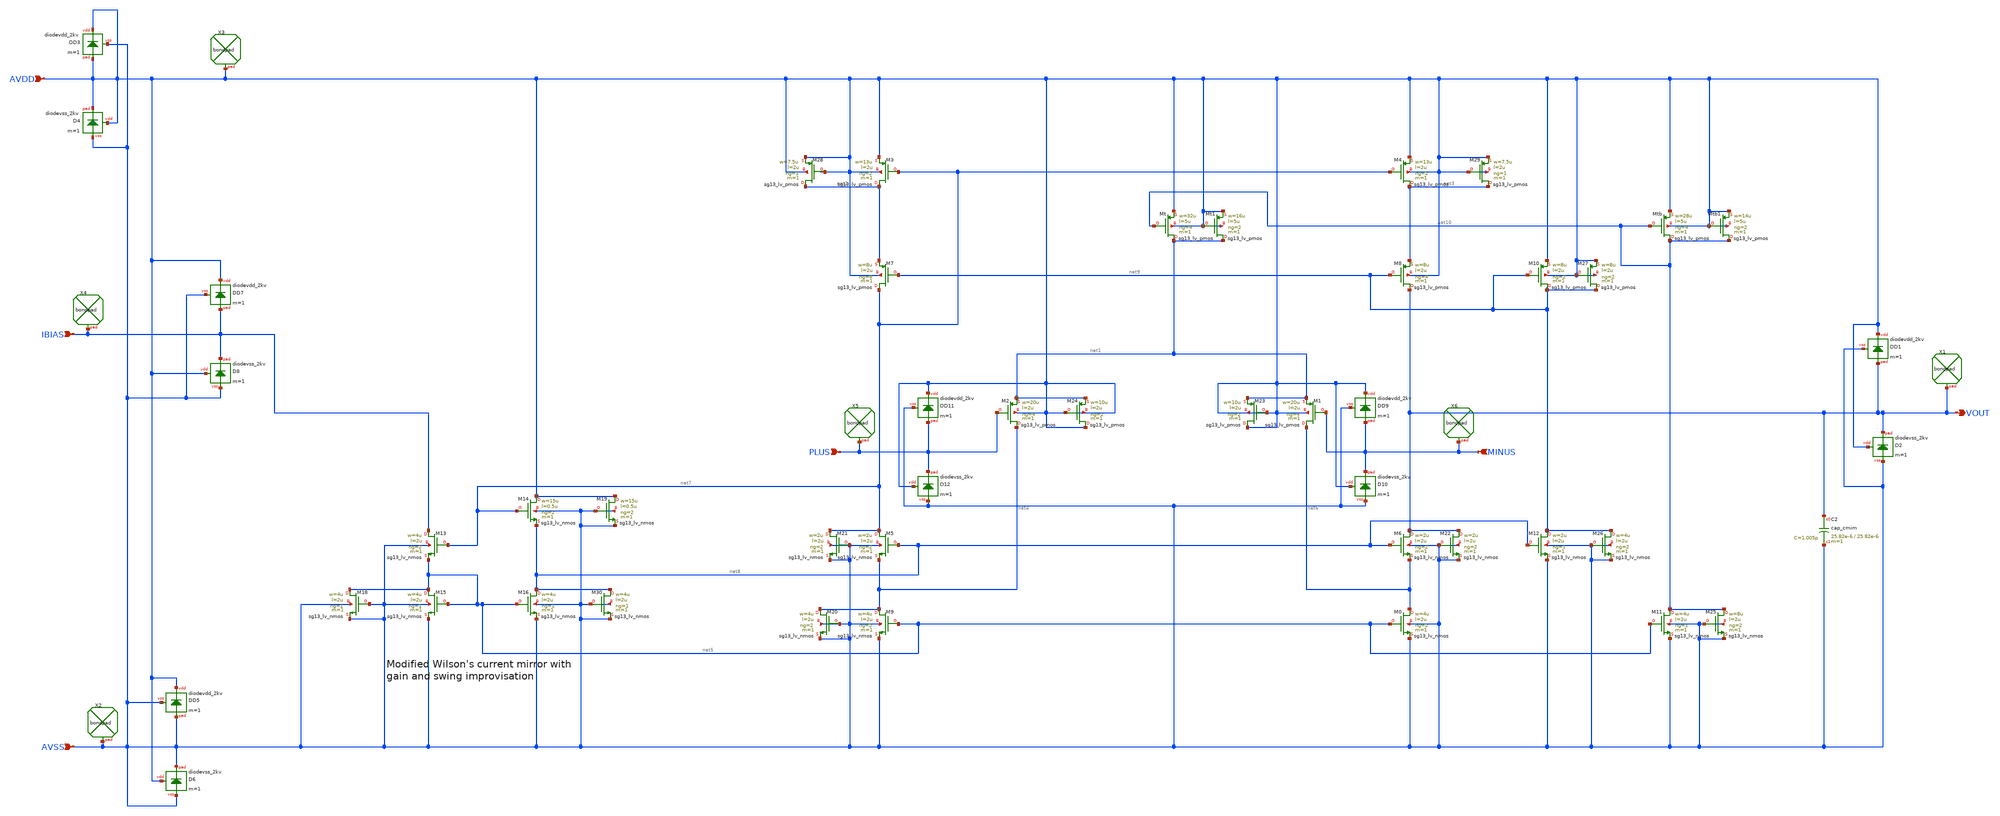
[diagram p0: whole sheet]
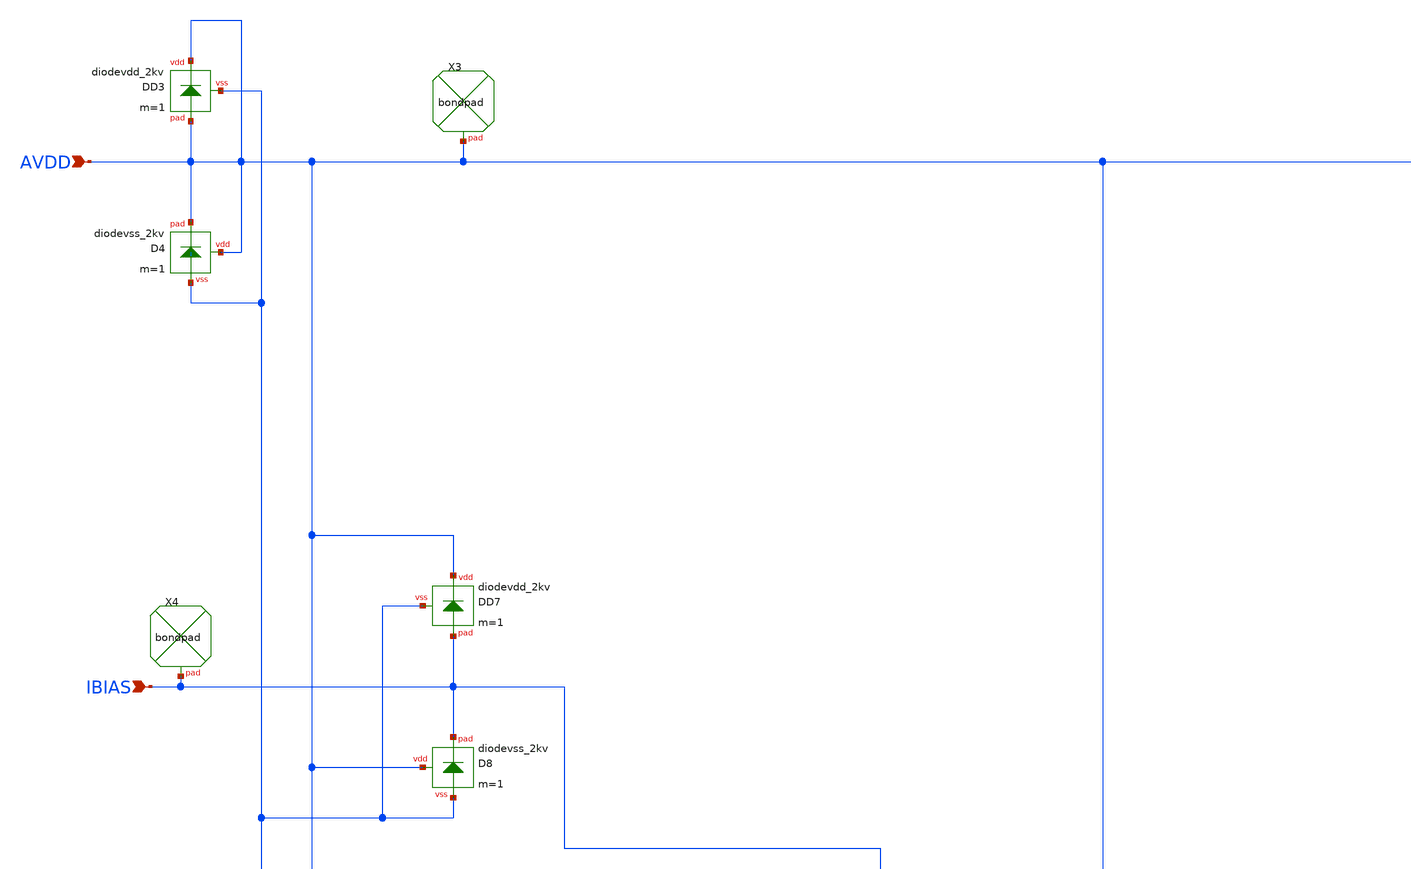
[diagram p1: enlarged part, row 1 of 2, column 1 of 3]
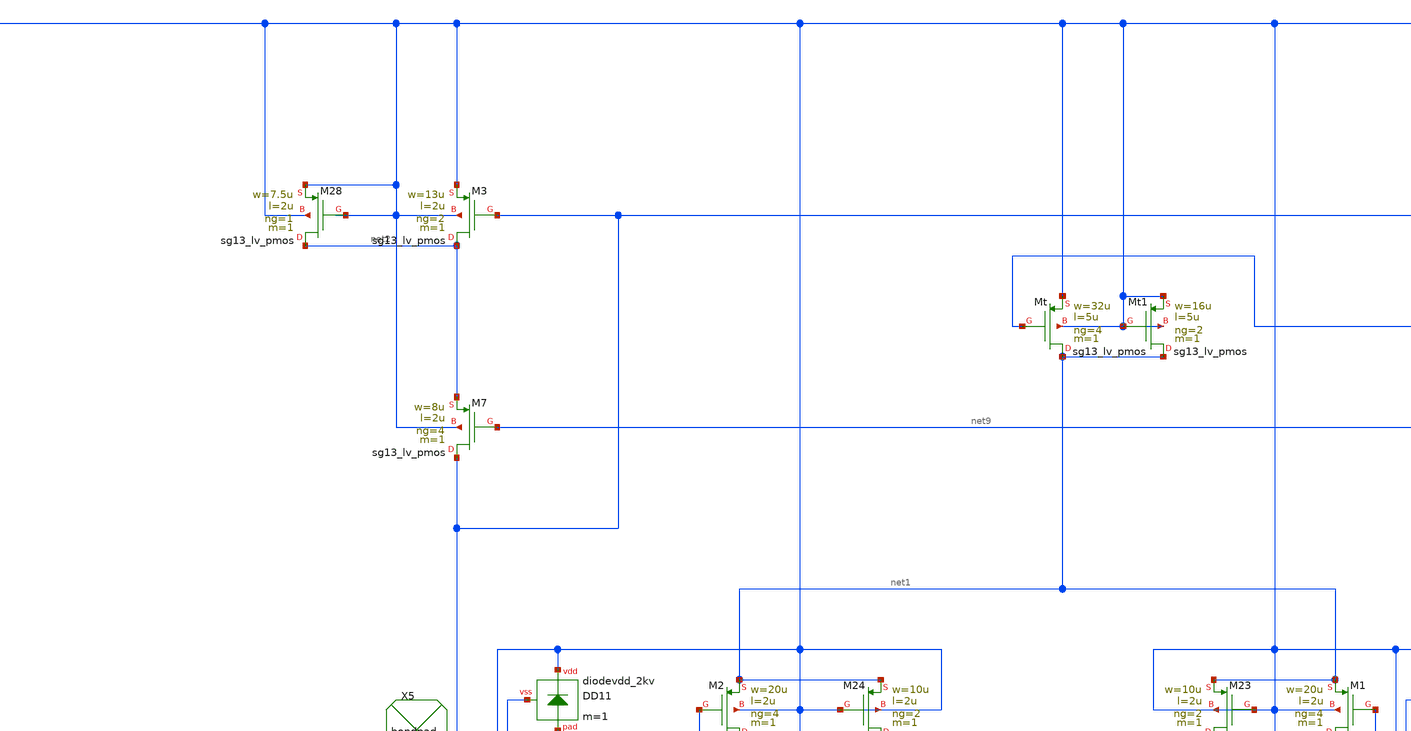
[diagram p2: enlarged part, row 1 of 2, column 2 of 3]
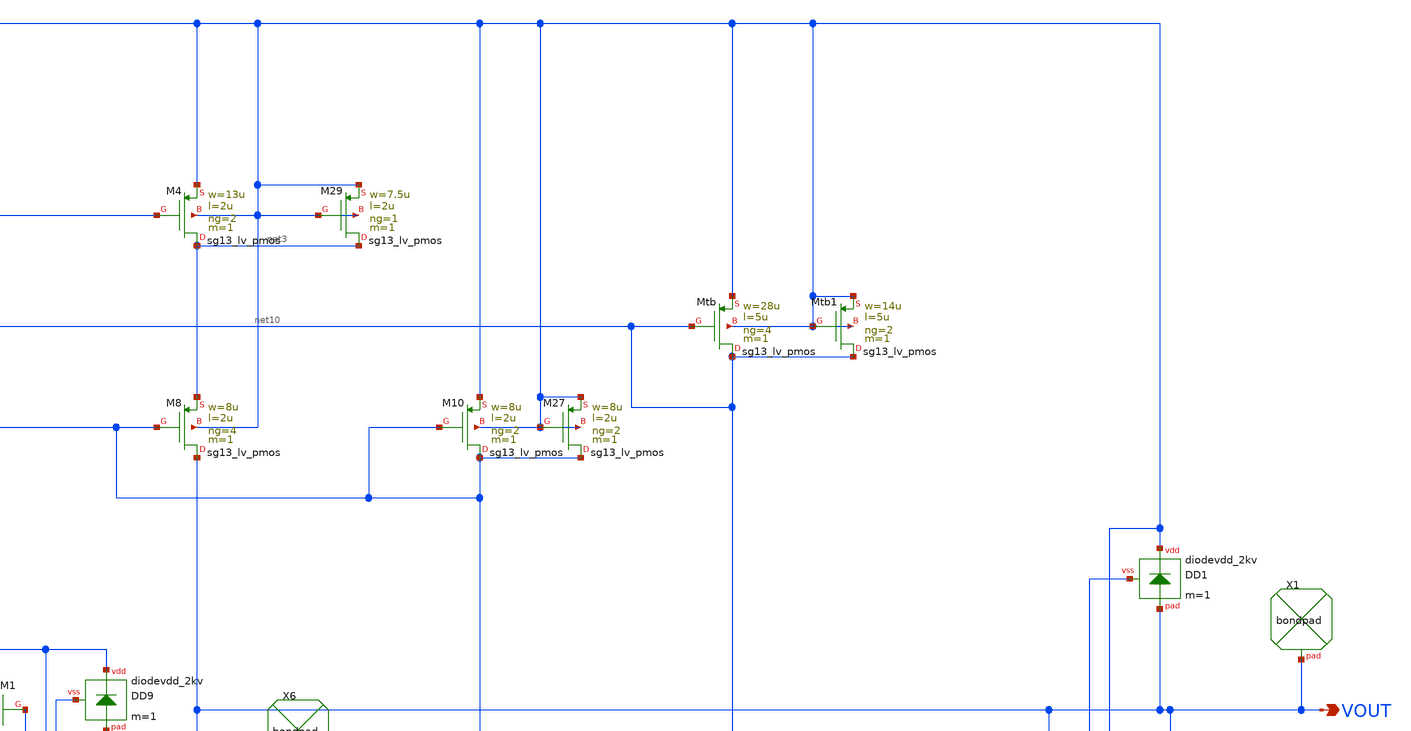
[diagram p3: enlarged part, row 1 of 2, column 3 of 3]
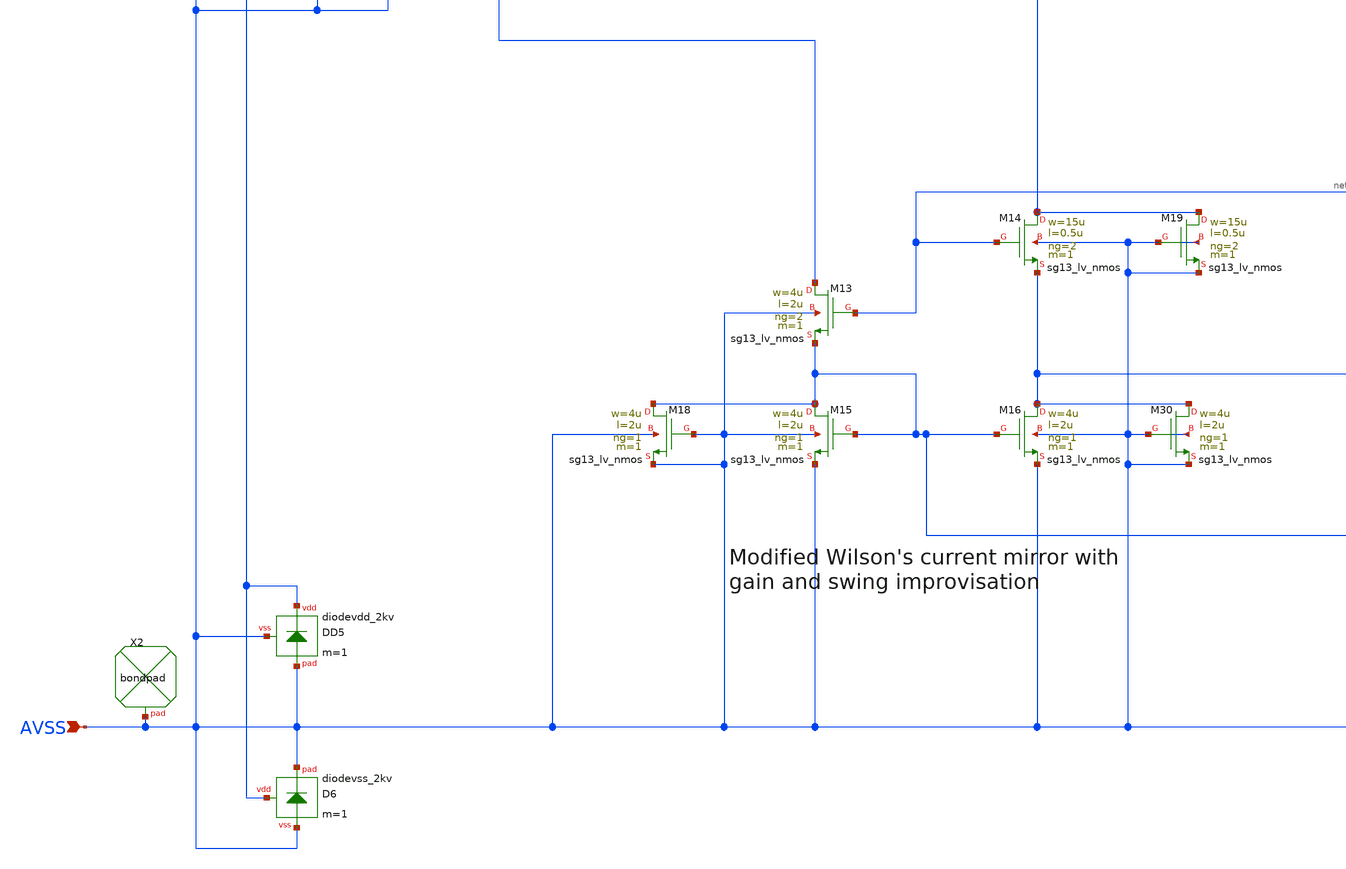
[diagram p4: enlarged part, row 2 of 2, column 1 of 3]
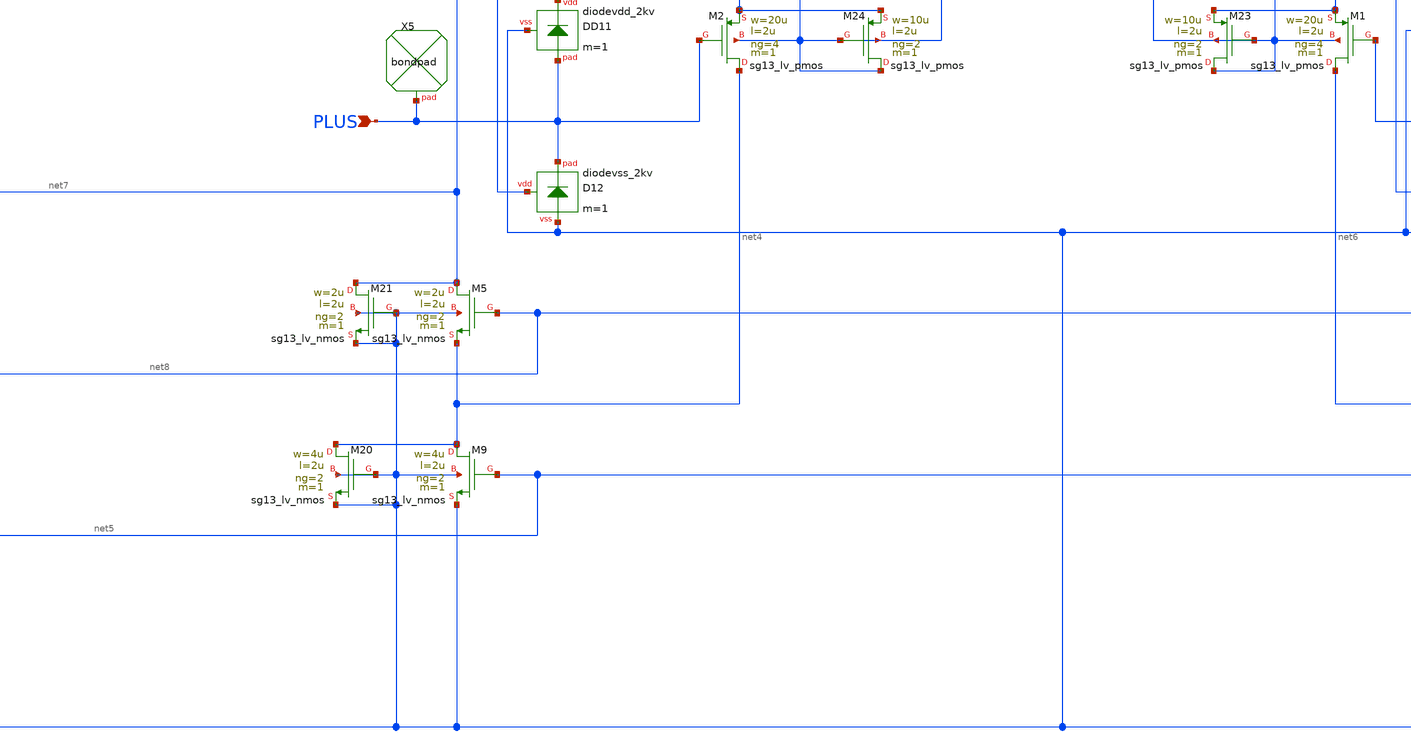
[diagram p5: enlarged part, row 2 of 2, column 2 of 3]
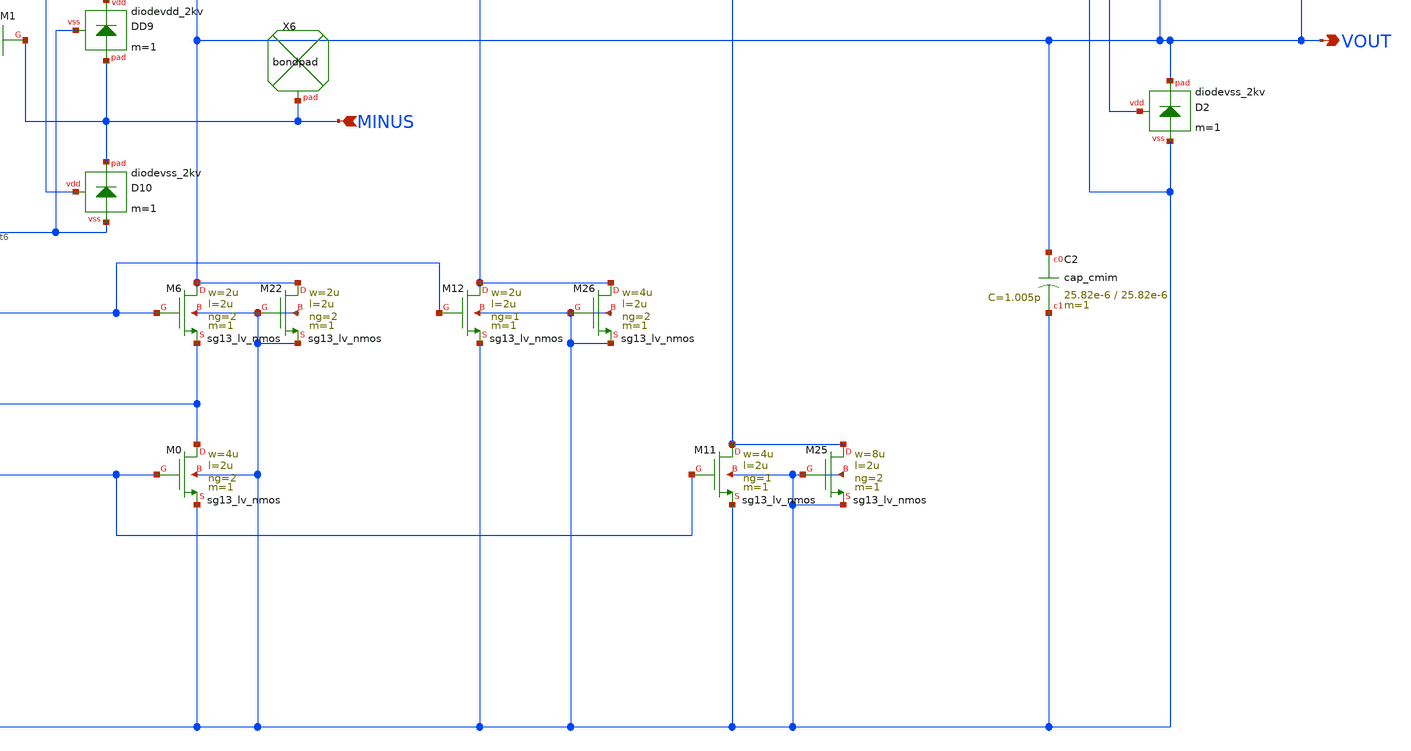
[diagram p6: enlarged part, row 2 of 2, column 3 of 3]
** sch_path: Designs/otas/1_schematics/foldedcascode_pmos_with_pmos_dummy.sch
**.subckt foldedcascode_pmos_with_pmos_dummy PLUS MINUS AVSS IBIAS AVDD VOUT
*.ipin PLUS
*.ipin MINUS
*.ipin AVSS
*.ipin IBIAS
*.ipin AVDD
*.opin VOUT
XM1 net6 MINUS net1 AVDD sg13_lv_pmos w=20u l=2u ng=4 m=1 mm_ok=1
XM5 net7 net8 net4 AVSS sg13_lv_nmos w=2u l=2u ng=2 m=1 mm_ok=1
XM2 net4 PLUS net1 AVDD sg13_lv_pmos w=20u l=2u ng=4 m=1 mm_ok=1
XM3 net2 net7 AVDD AVDD sg13_lv_pmos w=13u l=2u ng=2 m=1 mm_ok=1
XM4 net3 net7 AVDD AVDD sg13_lv_pmos w=13u l=2u ng=2 m=1 mm_ok=1
XM7 net7 net9 net2 AVDD sg13_lv_pmos w=8u l=2u ng=4 m=1 mm_ok=1
XM8 VOUT net9 net3 AVDD sg13_lv_pmos w=8u l=2u ng=4 m=1 mm_ok=1
XM6 VOUT net8 net6 AVSS sg13_lv_nmos w=2u l=2u ng=2 m=1 mm_ok=1
XM9 net4 net5 AVSS AVSS sg13_lv_nmos w=4u l=2u ng=2 m=1 mm_ok=1
XM0 net6 net5 AVSS AVSS sg13_lv_nmos w=4u l=2u ng=2 m=1 mm_ok=1
XMt net1 net10 AVDD AVDD sg13_lv_pmos w=32u l=5u ng=4 m=1 mm_ok=1
XM13 IBIAS net7 net5 AVSS sg13_lv_nmos w=4u l=2u ng=2 m=1 mm_ok=1
XM15 net5 net5 AVSS AVSS sg13_lv_nmos w=4u l=2u ng=1 m=1 mm_ok=1
XM16 net8 net5 AVSS AVSS sg13_lv_nmos w=4u l=2u ng=1 m=1 mm_ok=1
XM14 AVDD net7 net8 AVSS sg13_lv_nmos w=15u l=0.5u ng=2 m=1 mm_ok=1
XM12 net9 net8 AVSS AVSS sg13_lv_nmos w=2u l=2u ng=1 m=1 mm_ok=1
XM10 net9 net9 AVDD AVDD sg13_lv_pmos w=8u l=2u ng=2 m=1 mm_ok=1
XM11 net10 net5 AVSS AVSS sg13_lv_nmos w=4u l=2u ng=1 m=1 mm_ok=1
XMtb net10 net10 AVDD AVDD sg13_lv_pmos w=28u l=5u ng=4 m=1 mm_ok=1
XM18 net5 AVSS AVSS AVSS sg13_lv_nmos w=4u l=2u ng=1 m=1 mm_ok=1
XM19 AVDD AVSS AVSS AVSS sg13_lv_nmos w=15u l=0.5u ng=2 m=1 mm_ok=1
XM20 net4 AVSS AVSS AVSS sg13_lv_nmos w=4u l=2u ng=2 m=1 mm_ok=1
XM21 net7 AVSS AVSS AVSS sg13_lv_nmos w=2u l=2u ng=2 m=1 mm_ok=1
XM22 VOUT AVSS AVSS AVSS sg13_lv_nmos w=2u l=2u ng=2 m=1 mm_ok=1
XM23 AVDD AVDD net1 AVDD sg13_lv_pmos w=10u l=2u ng=2 m=1 mm_ok=1
XM24 AVDD AVDD net1 AVDD sg13_lv_pmos w=10u l=2u ng=2 m=1 mm_ok=1
XM25 net10 AVSS AVSS AVSS sg13_lv_nmos w=8u l=2u ng=2 m=1 mm_ok=1
XM26 net9 AVSS AVSS AVSS sg13_lv_nmos w=4u l=2u ng=2 m=1 mm_ok=1
XMtb1 net10 AVDD AVDD AVDD sg13_lv_pmos w=14u l=5u ng=2 m=1 mm_ok=1
XM27 net9 AVDD AVDD AVDD sg13_lv_pmos w=8u l=2u ng=2 m=1 mm_ok=1
XMt1 net1 AVDD AVDD AVDD sg13_lv_pmos w=16u l=5u ng=2 m=1 mm_ok=1
XM28 net2 AVDD AVDD AVDD sg13_lv_pmos w=7.5u l=2u ng=1 m=1 mm_ok=1
XM29 net3 AVDD AVDD AVDD sg13_lv_pmos w=7.5u l=2u ng=1 m=1 mm_ok=1
XD3 AVDD AVDD AVSS diodevdd_2kv m=1
XD4 AVDD AVDD AVSS diodevss_2kv m=1
XD5 AVDD AVSS AVSS diodevdd_2kv m=1
XD6 AVDD AVSS AVSS diodevss_2kv m=1
XX2 AVSS bondpad size=80u shape=0 padtype=0
XX3 AVDD bondpad size=80u shape=0 padtype=0
XD7 AVDD IBIAS AVSS diodevdd_2kv m=1
XD8 AVDD IBIAS AVSS diodevss_2kv m=1
XX4 IBIAS bondpad size=80u shape=0 padtype=0
XC2 VOUT AVSS cap_cmim w=25.82e-6 l=25.82e-6 m=1 mm_ok=1
XX1 VOUT bondpad size=80u shape=0 padtype=0
XD1 AVDD VOUT AVSS diodevdd_2kv m=1
XD2 AVDD VOUT AVSS diodevss_2kv m=1
XX5 PLUS bondpad size=80u shape=0 padtype=0
XX6 MINUS bondpad size=80u shape=0 padtype=0
XD11 AVDD PLUS AVSS diodevdd_2kv m=1
XD9 AVDD MINUS AVSS diodevdd_2kv m=1
XD12 AVDD PLUS AVSS diodevss_2kv m=1
XD10 AVDD MINUS AVSS diodevss_2kv m=1
XM30 net8 AVSS AVSS AVSS sg13_lv_nmos w=4u l=2u ng=1 m=1 mm_ok=1
**.ends
.end
